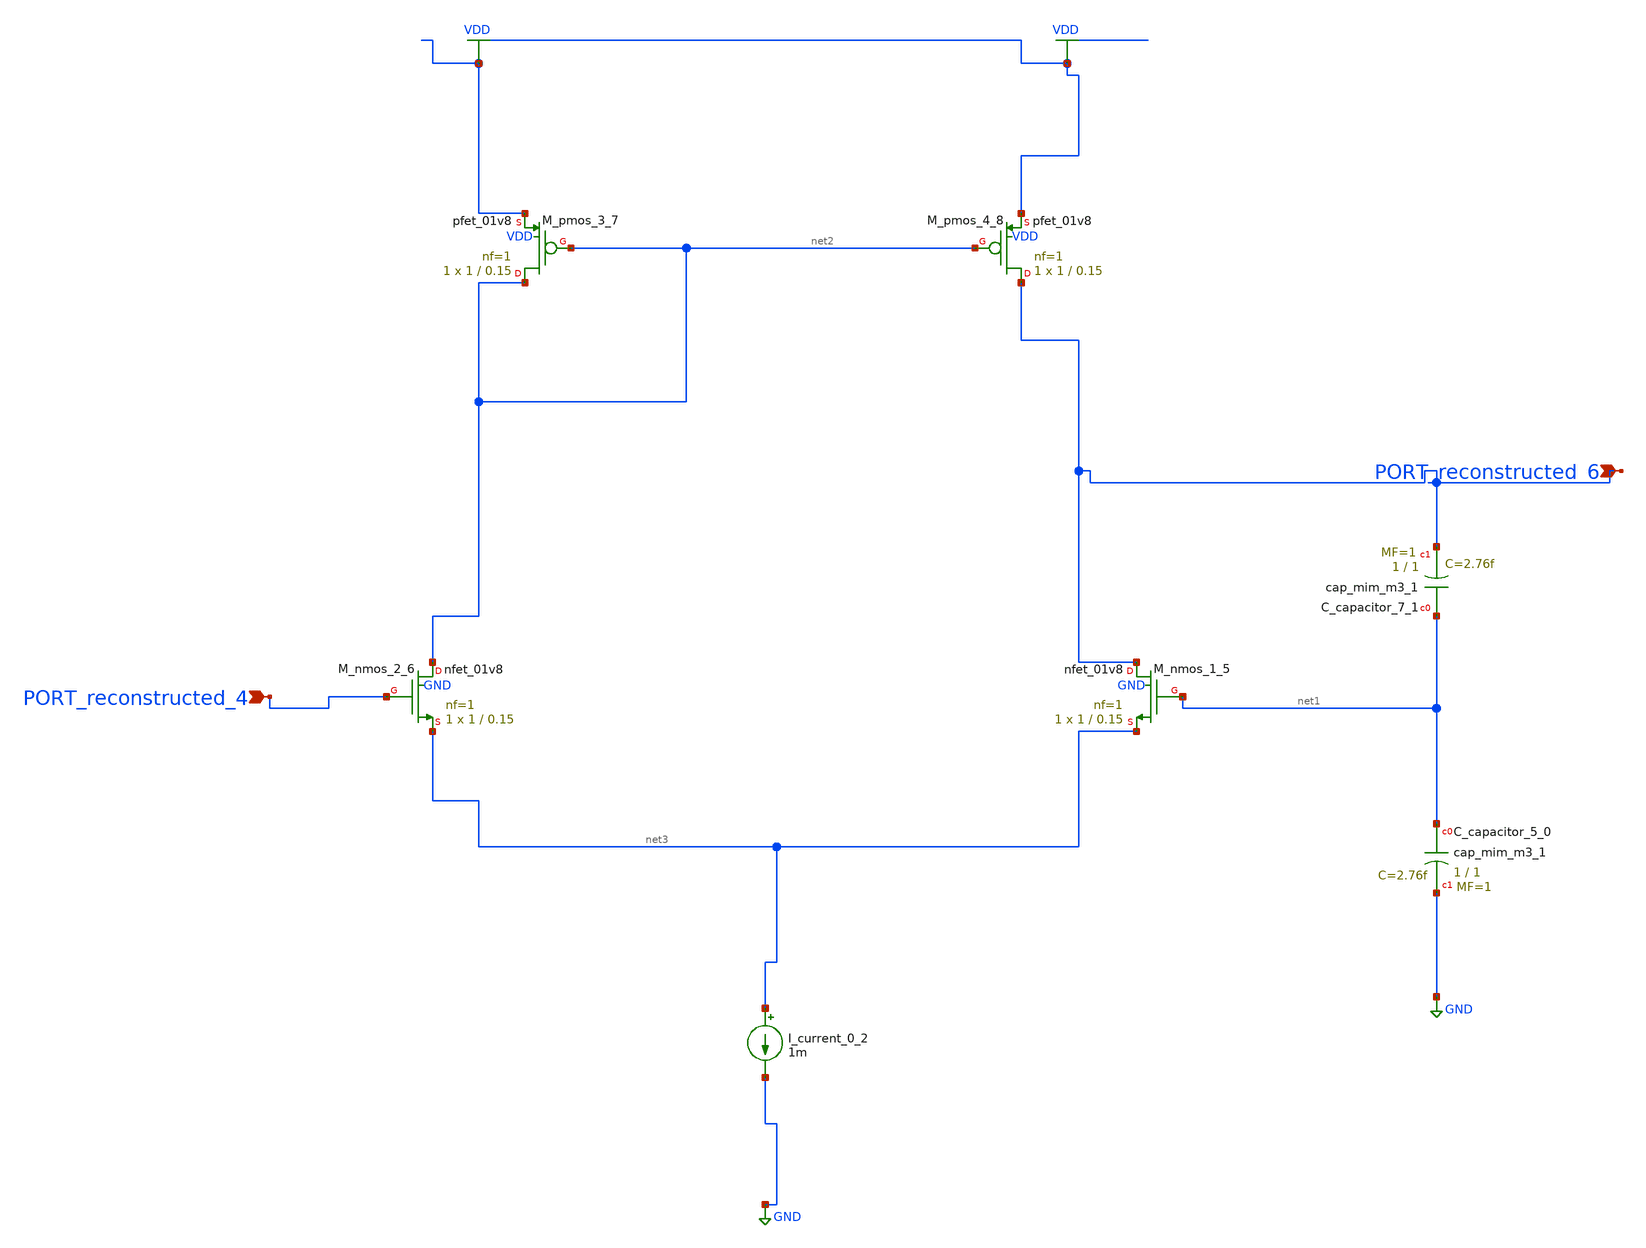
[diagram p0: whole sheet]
** sch_path: schematics/AMSNet/689.sch
**.subckt 689 PORT_reconstructed_6 PORT_reconstructed_4
*.ipin PORT_reconstructed_6
*.ipin PORT_reconstructed_4
XC_capacitor_5_0 net1 GND sky130_fd_pr__cap_mim_m3_1 W=1 L=1 MF=1 m=1
XC_capacitor_7_1 net1 PORT_reconstructed_6 sky130_fd_pr__cap_mim_m3_1 W=1 L=1 MF=1 m=1
I_current_0_2 net3 GND 1m
XM_nmos_1_5 PORT_reconstructed_6 net1 net3 GND sky130_fd_pr__nfet_01v8 L=0.15 W=1 nf=1 ad='int((1 + 1)/2) * 1 / 1 * 0.29'
+ as='int((1 + 2)/2) * 1 / 1 * 0.29' pd='2*int((1 + 1)/2) * (1 / 1 + 0.29)' ps='2*int((1 + 2)/2) * (1 / 1 + 0.29)'
+ nrd='0.29 / 1 ' nrs='0.29 / 1 ' sa=0 sb=0 sd=0 mult=1 m=1
XM_nmos_2_6 net2 PORT_reconstructed_4 net3 GND sky130_fd_pr__nfet_01v8 L=0.15 W=1 nf=1 ad='int((1 + 1)/2) * 1 / 1 * 0.29'
+ as='int((1 + 2)/2) * 1 / 1 * 0.29' pd='2*int((1 + 1)/2) * (1 / 1 + 0.29)' ps='2*int((1 + 2)/2) * (1 / 1 + 0.29)'
+ nrd='0.29 / 1 ' nrs='0.29 / 1 ' sa=0 sb=0 sd=0 mult=1 m=1
XM_pmos_3_7 net2 net2 VDD VDD sky130_fd_pr__pfet_01v8 L=0.15 W=1 nf=1 ad='int((1 + 1)/2) * 1 / 1 * 0.29'
+ as='int((1 + 2)/2) * 1 / 1 * 0.29' pd='2*int((1 + 1)/2) * (1 / 1 + 0.29)' ps='2*int((1 + 2)/2) * (1 / 1 + 0.29)'
+ nrd='0.29 / 1 ' nrs='0.29 / 1 ' sa=0 sb=0 sd=0 mult=1 m=1
XM_pmos_4_8 PORT_reconstructed_6 net2 VDD VDD sky130_fd_pr__pfet_01v8 L=0.15 W=1 nf=1 ad='int((1 + 1)/2) * 1 / 1 * 0.29'
+ as='int((1 + 2)/2) * 1 / 1 * 0.29' pd='2*int((1 + 1)/2) * (1 / 1 + 0.29)' ps='2*int((1 + 2)/2) * (1 / 1 + 0.29)'
+ nrd='0.29 / 1 ' nrs='0.29 / 1 ' sa=0 sb=0 sd=0 mult=1 m=1
**.ends
.GLOBAL GND
.GLOBAL VDD
.end
